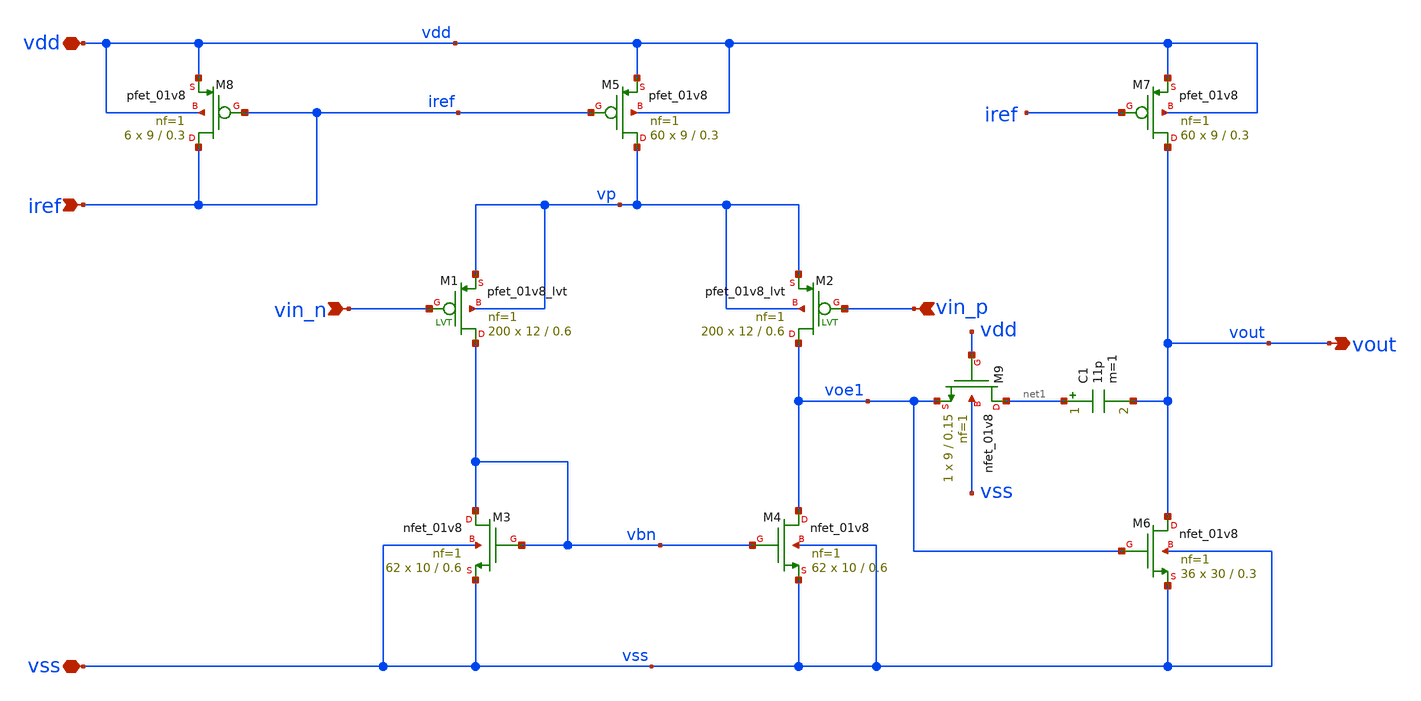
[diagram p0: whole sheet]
** sch_path: xschem/opamp.sch
**.subckt opamp vdd vss vin_n vin_p iref vout
*.iopin vdd
*.iopin vss
*.ipin vin_n
*.ipin vin_p
*.ipin iref
*.opin vout
XM3 vbn vbn vss vss sky130_fd_pr__nfet_01v8 L=0.6 W=10 nf=1 ad='W * 0.29' as='W * 0.29' pd='2 * (W + 0.29)'
+ ps='2 * (W + 0.29)' nrd='0.29 / W' nrs='0.29 / W' sa=0 sb=0 sd=0 mult=62 m=62
XM4 voe1 vbn vss vss sky130_fd_pr__nfet_01v8 L=0.6 W=10 nf=1 ad='W * 0.29' as='W * 0.29' pd='2 * (W + 0.29)'
+ ps='2 * (W + 0.29)' nrd='0.29 / W' nrs='0.29 / W' sa=0 sb=0 sd=0 mult=62 m=62
XM5 vp iref vdd vdd sky130_fd_pr__pfet_01v8 L=0.3 W=9 nf=1 ad='W * 0.29' as='W * 0.29' pd='2 * (W + 0.29)'
+ ps='2 * (W + 0.29)' nrd='0.29 / W' nrs='0.29 / W' sa=0 sb=0 sd=0 mult=60 m=60
XM7 vout iref vdd vdd sky130_fd_pr__pfet_01v8 L=0.3 W=9 nf=1 ad='W * 0.29' as='W * 0.29' pd='2 * (W + 0.29)'
+ ps='2 * (W + 0.29)' nrd='0.29 / W' nrs='0.29 / W' sa=0 sb=0 sd=0 mult=60 m=60
XM8 iref iref vdd vdd sky130_fd_pr__pfet_01v8 L=0.3 W=9 nf=1 ad='W * 0.29' as='W * 0.29' pd='2 * (W + 0.29)'
+ ps='2 * (W + 0.29)' nrd='0.29 / W' nrs='0.29 / W' sa=0 sb=0 sd=0 mult=6 m=6
XM9 net1 vdd voe1 vss sky130_fd_pr__nfet_01v8 L=0.15 W=9 nf=1 ad='W * 0.29' as='W * 0.29' pd='2 * (W + 0.29)'
+ ps='2 * (W + 0.29)' nrd='0.29 / W' nrs='0.29 / W' sa=0 sb=0 sd=0 mult=1 m=1
XM6 vout voe1 vss vss sky130_fd_pr__nfet_01v8 L=0.3 W=30 nf=1 ad='W * 0.29' as='W * 0.29' pd='2 * (W + 0.29)'
+ ps='2 * (W + 0.29)' nrd='0.29 / W' nrs='0.29 / W' sa=0 sb=0 sd=0 mult=36 m=36
XM1 vbn vin_n vp vp sky130_fd_pr__pfet_01v8_lvt L=0.6 W=12 nf=1 ad='int((nf+1)/2) * W/nf * 0.29' as='int((nf+2)/2) * W/nf * 0.29'
+ pd='2*int((nf+1)/2) * (W/nf + 0.29)' ps='2*int((nf+2)/2) * (W/nf + 0.29)' nrd='0.29 / W' nrs='0.29 / W'
+ sa=0 sb=0 sd=0 mult=200 m=200
XM2 voe1 vin_p vp vp sky130_fd_pr__pfet_01v8_lvt L=0.6 W=12 nf=1 ad='int((nf+1)/2) * W/nf * 0.29' as='int((nf+2)/2) * W/nf * 0.29'
+ pd='2*int((nf+1)/2) * (W/nf + 0.29)' ps='2*int((nf+2)/2) * (W/nf + 0.29)' nrd='0.29 / W' nrs='0.29 / W'
+ sa=0 sb=0 sd=0 mult=200 m=200
C1 net1 vout 11p m=1
**.ends
.end
